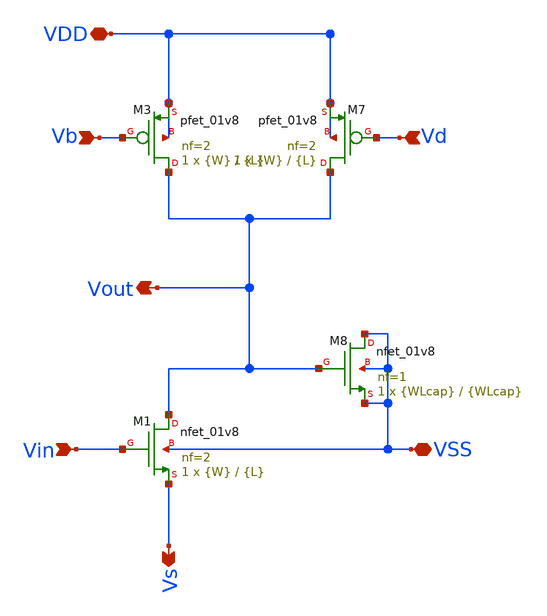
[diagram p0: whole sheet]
** sch_path: xschem/vco_stage_half.sch
**.subckt vco_stage_half VDD VSS Vin Vb Vd Vout Vs
*.iopin VDD
*.iopin VSS
*.ipin Vin
*.ipin Vb
*.ipin Vd
*.opin Vout
*.opin Vs
XM8 VSS Vout VSS VSS sky130_fd_pr__nfet_01v8 L={WLcap} W={WLcap} nf=1 ad='int((nf+1)/2) * W/nf * 0.29'
+ as='int((nf+2)/2) * W/nf * 0.29' pd='2*int((nf+1)/2) * (W/nf + 0.29)' ps='2*int((nf+2)/2) * (W/nf + 0.29)'
+ nrd='0.29 / W' nrs='0.29 / W' sa=0 sb=0 sd=0 mult=1 m=1
XM7 Vout Vd VDD VDD sky130_fd_pr__pfet_01v8 L={L} W={W} nf=2 ad='int((nf+1)/2) * W/nf * 0.29' as='int((nf+2)/2) * W/nf * 0.29'
+ pd='2*int((nf+1)/2) * (W/nf + 0.29)' ps='2*int((nf+2)/2) * (W/nf + 0.29)' nrd='0.29 / W' nrs='0.29 / W'
+ sa=0 sb=0 sd=0 mult=1 m=1
XM3 Vout Vb VDD VDD sky130_fd_pr__pfet_01v8 L={L} W={W} nf=2 ad='int((nf+1)/2) * W/nf * 0.29' as='int((nf+2)/2) * W/nf * 0.29'
+ pd='2*int((nf+1)/2) * (W/nf + 0.29)' ps='2*int((nf+2)/2) * (W/nf + 0.29)' nrd='0.29 / W' nrs='0.29 / W'
+ sa=0 sb=0 sd=0 mult=1 m=1
XM1 Vout Vin Vs VSS sky130_fd_pr__nfet_01v8 L={L} W={W} nf=2 ad='int((nf+1)/2) * W/nf * 0.29' as='int((nf+2)/2) * W/nf * 0.29'
+ pd='2*int((nf+1)/2) * (W/nf + 0.29)' ps='2*int((nf+2)/2) * (W/nf + 0.29)' nrd='0.29 / W' nrs='0.29 / W'
+ sa=0 sb=0 sd=0 mult=1 m=1
**.ends
.end
